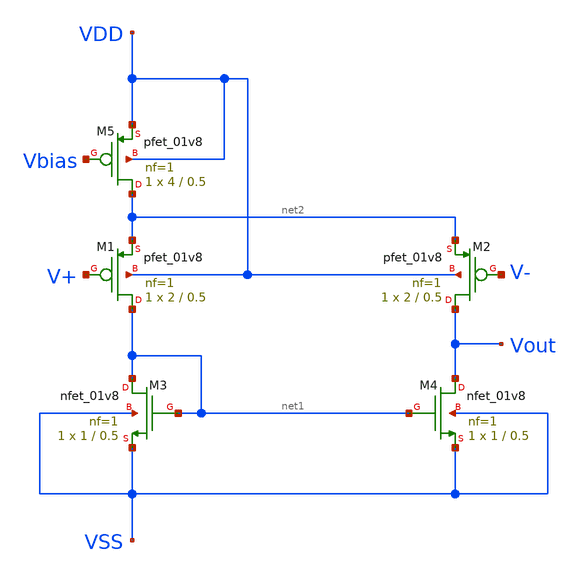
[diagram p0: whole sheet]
** sch_path: analog/schematics/bootcamp_opamp.sch
**.subckt bootcamp_opamp
XM5 net2 Vbias VDD VDD sky130_fd_pr__pfet_01v8 L=0.5 W=4 nf=1 ad='int((nf+1)/2) * W/nf * 0.29' as='int((nf+2)/2) * W/nf * 0.29'
+ pd='2*int((nf+1)/2) * (W/nf + 0.29)' ps='2*int((nf+2)/2) * (W/nf + 0.29)' nrd='0.29 / W' nrs='0.29 / W'
+ sa=0 sb=0 sd=0 mult=1 m=1
XM1 net1 V+ net2 VDD sky130_fd_pr__pfet_01v8 L=0.5 W=2 nf=1 ad='int((nf+1)/2) * W/nf * 0.29' as='int((nf+2)/2) * W/nf * 0.29'
+ pd='2*int((nf+1)/2) * (W/nf + 0.29)' ps='2*int((nf+2)/2) * (W/nf + 0.29)' nrd='0.29 / W' nrs='0.29 / W'
+ sa=0 sb=0 sd=0 mult=1 m=1
XM2 Vout V- net2 VDD sky130_fd_pr__pfet_01v8 L=0.5 W=2 nf=1 ad='int((nf+1)/2) * W/nf * 0.29' as='int((nf+2)/2) * W/nf * 0.29'
+ pd='2*int((nf+1)/2) * (W/nf + 0.29)' ps='2*int((nf+2)/2) * (W/nf + 0.29)' nrd='0.29 / W' nrs='0.29 / W'
+ sa=0 sb=0 sd=0 mult=1 m=1
XM3 net1 net1 VSS VSS sky130_fd_pr__nfet_01v8 L=0.5 W=1 nf=1 ad='int((nf+1)/2) * W/nf * 0.29' as='int((nf+2)/2) * W/nf * 0.29'
+ pd='2*int((nf+1)/2) * (W/nf + 0.29)' ps='2*int((nf+2)/2) * (W/nf + 0.29)' nrd='0.29 / W' nrs='0.29 / W'
+ sa=0 sb=0 sd=0 mult=1 m=1
XM4 Vout net1 VSS VSS sky130_fd_pr__nfet_01v8 L=0.5 W=1 nf=1 ad='int((nf+1)/2) * W/nf * 0.29' as='int((nf+2)/2) * W/nf * 0.29'
+ pd='2*int((nf+1)/2) * (W/nf + 0.29)' ps='2*int((nf+2)/2) * (W/nf + 0.29)' nrd='0.29 / W' nrs='0.29 / W'
+ sa=0 sb=0 sd=0 mult=1 m=1
**.ends
.end
